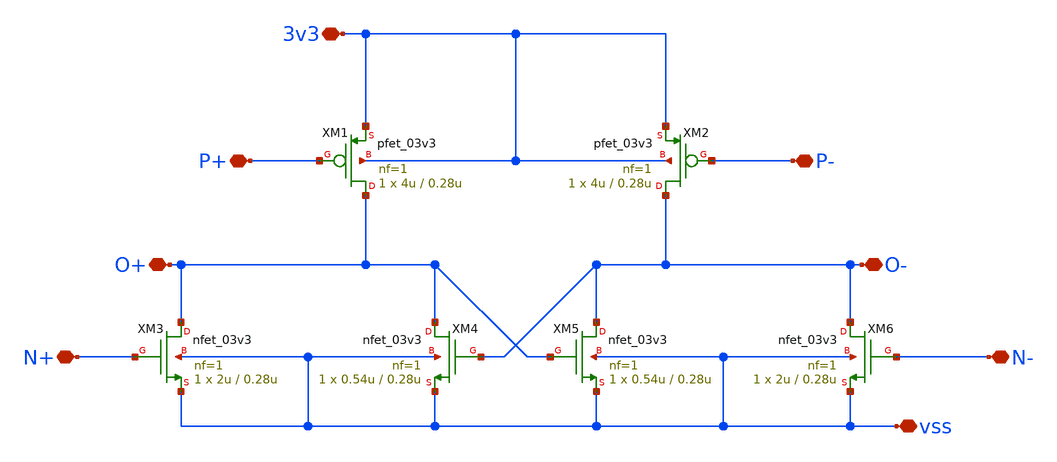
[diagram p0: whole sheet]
** sch_path: PLL/analog/schematics/Differential_Stage_DAC_Core.sch
**.subckt Differential_Stage_DAC_Core P+ P- N+ N- vss 3v3 O+ O-
*.iopin P+
*.iopin P-
*.iopin N+
*.iopin N-
*.iopin vss
*.iopin 3v3
*.iopin O+
*.iopin O-
XM1 O+ P+ 3v3 3v3 pfet_03v3 L=0.28u W=4u nf=1 ad='int((nf+1)/2) * W/nf * 0.18u' as='int((nf+2)/2) * W/nf * 0.18u'
+ pd='2*int((nf+1)/2) * (W/nf + 0.18u)' ps='2*int((nf+2)/2) * (W/nf + 0.18u)' nrd='0.18u / W' nrs='0.18u / W'
+ sa=0 sb=0 sd=0 m=1
XM2 O- P- 3v3 3v3 pfet_03v3 L=0.28u W=4u nf=1 ad='int((nf+1)/2) * W/nf * 0.18u' as='int((nf+2)/2) * W/nf * 0.18u'
+ pd='2*int((nf+1)/2) * (W/nf + 0.18u)' ps='2*int((nf+2)/2) * (W/nf + 0.18u)' nrd='0.18u / W' nrs='0.18u / W'
+ sa=0 sb=0 sd=0 m=1
XM3 O+ N+ vss vss nfet_03v3 L=0.28u W=2u nf=1 ad='int((nf+1)/2) * W/nf * 0.18u' as='int((nf+2)/2) * W/nf * 0.18u'
+ pd='2*int((nf+1)/2) * (W/nf + 0.18u)' ps='2*int((nf+2)/2) * (W/nf + 0.18u)' nrd='0.18u / W' nrs='0.18u / W'
+ sa=0 sb=0 sd=0 m=1
XM4 O+ O- vss vss nfet_03v3 L=0.28u W=0.54u nf=1 ad='int((nf+1)/2) * W/nf * 0.18u' as='int((nf+2)/2) * W/nf * 0.18u'
+ pd='2*int((nf+1)/2) * (W/nf + 0.18u)' ps='2*int((nf+2)/2) * (W/nf + 0.18u)' nrd='0.18u / W' nrs='0.18u / W'
+ sa=0 sb=0 sd=0 m=1
XM5 O- O+ vss vss nfet_03v3 L=0.28u W=0.54u nf=1 ad='int((nf+1)/2) * W/nf * 0.18u' as='int((nf+2)/2) * W/nf * 0.18u'
+ pd='2*int((nf+1)/2) * (W/nf + 0.18u)' ps='2*int((nf+2)/2) * (W/nf + 0.18u)' nrd='0.18u / W' nrs='0.18u / W'
+ sa=0 sb=0 sd=0 m=1
XM6 O- N- vss vss nfet_03v3 L=0.28u W=2u nf=1 ad='int((nf+1)/2) * W/nf * 0.18u' as='int((nf+2)/2) * W/nf * 0.18u'
+ pd='2*int((nf+1)/2) * (W/nf + 0.18u)' ps='2*int((nf+2)/2) * (W/nf + 0.18u)' nrd='0.18u / W' nrs='0.18u / W'
+ sa=0 sb=0 sd=0 m=1
**.ends
.end
